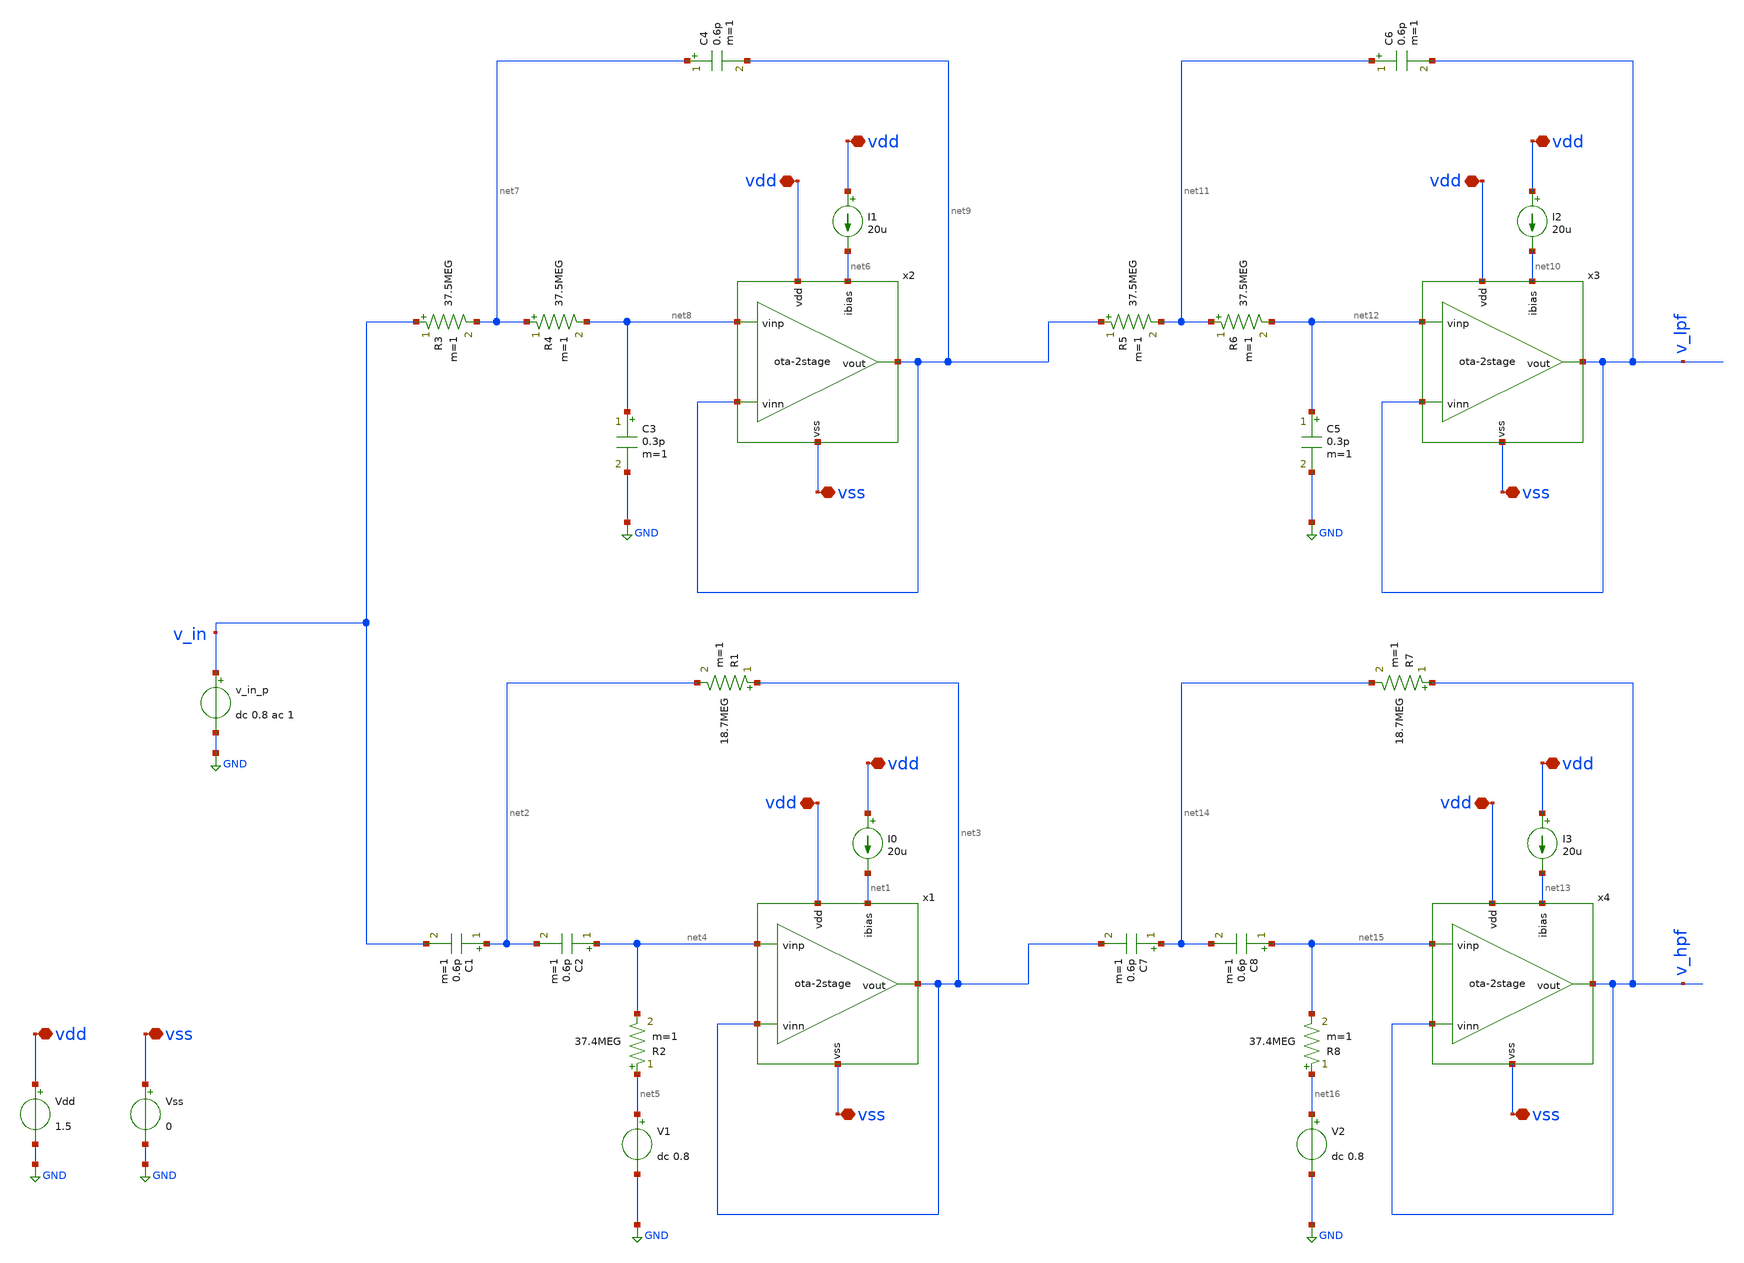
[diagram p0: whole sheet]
** sch_path: xschem/ota-2stage_tb-sk-LR4.sch
**.subckt ota-2stage_tb-sk-LR4 vdd vdd vdd vss vss vdd vdd vss vdd vdd vss vdd vdd vss
*.iopin vdd
*.iopin vdd
*.iopin vdd
*.iopin vss
*.iopin vss
*.iopin vdd
*.iopin vdd
*.iopin vss
*.iopin vdd
*.iopin vdd
*.iopin vss
*.iopin vdd
*.iopin vdd
*.iopin vss
I0 vdd net1 20u
Vdd vdd GND 1.5
Vss vss GND 0
v_in_p v_in GND dc 0.8 ac 1
x1 vdd net1 net3 net3 net4 vss ota-2stage
R1 net3 net2 18.7MEG m=1
R2 net5 net4 37.4MEG m=1
C1 net2 v_in 0.6p m=1
C2 net4 net2 0.6p m=1
V1 net5 GND dc 0.8
I1 vdd net6 20u
R3 v_in net7 37.5MEG m=1
R4 net7 net8 37.5MEG m=1
C3 net8 GND 0.3p m=1
C4 net7 net9 0.6p m=1
x2 vdd net6 net9 net9 net8 vss ota-2stage
I2 vdd net10 20u
R5 net9 net11 37.5MEG m=1
R6 net11 net12 37.5MEG m=1
C5 net12 GND 0.3p m=1
C6 net11 v_lpf 0.6p m=1
x3 vdd net10 v_lpf v_lpf net12 vss ota-2stage
I3 vdd net13 20u
x4 vdd net13 v_hpf v_hpf net15 vss ota-2stage
R7 v_hpf net14 18.7MEG m=1
R8 net16 net15 37.4MEG m=1
C7 net14 net3 0.6p m=1
C8 net15 net14 0.6p m=1
V2 net16 GND dc 0.8
**** begin user architecture code


.temp 27
.control
option sparse
save all

* Sweep from 100 Hz to 1 MHz
ac dec 101 100 1MEG

* Plot the response to see 10kHz cutoff
let LPF = 20*log10(v(v_lpf))
let HPF = 20*log10(v(v_hpf))
let SUM = 20*log10(mag(v(v_lpf) + v(v_hpf)))
let DIF = 20*log10(mag(v(v_lpf) - v(v_hpf)))
plot LPF HPF SUM DIF title 'Frequency Responce'

set hcopydevtype=svg
hardcopy lr4_frequency_response.svg LPF HPF SUM DIF

let LPF_PHASE = vp(v_lpf)
let HPF_PHASE = vp(v_hpf)
plot LPF_PHASE HPF_PHASE title 'Phase Responce'

set hcopydevtype=svg
hardcopy lr4_phase_response.svg LPF_PHASE HPF_PHASE

* Measure the exact maximum DC gain of the Low-Pass section
meas ac max_gain MAX vmag(v_lpf) FROM=100 TO=1k

* For LR4, the crossover target is exactly half the voltage amplitude (-6dB)
let fc_target = max_gain / 2

* Find the exact frequency where the LPF drops to that target (-6dB)
meas ac crossover_freq WHEN vmag(v_lpf)=fc_target FALL=1

* 1. Find the voltage magnitudes at 100kHz and 1MHz
meas ac v_lpf_100k FIND vmag(v_lpf) AT=100k
meas ac v_lpf_1meg FIND vmag(v_lpf) AT=1MEG

* 2. Convert both points to dB and subtract to find the drop per decade
let db_lpf_100k = 20 * log10(v_lpf_100k)
let db_lpf_1meg = 20 * log10(v_lpf_1meg)
let slope_lpf = db_lpf_1meg - db_lpf_100k

* 1. Find the voltage magnitudes at 100Hz and 1kHz
meas ac v_hpf_100 FIND vmag(v_hpf) AT=100
meas ac v_hpf_1k   FIND vmag(v_hpf) AT=1k

* 2. Convert both points to dB and subtract to find the rise per decade
let db_hpf_100 = 20 * log10(v_hpf_100)
let db_hpf_1k   = 20 * log10(v_hpf_1k)
let slope_hpf = db_hpf_1k - db_hpf_100

print max_gain
print crossover_freq
print slope_lpf
print slope_hpf
.endc


 .lib cornerMOSlv.lib mos_tt
.lib cornerCAP.lib cap_typ
.lib cornerRES.lib res_typ

**** end user architecture code
**.ends
.GLOBAL GND
.end
